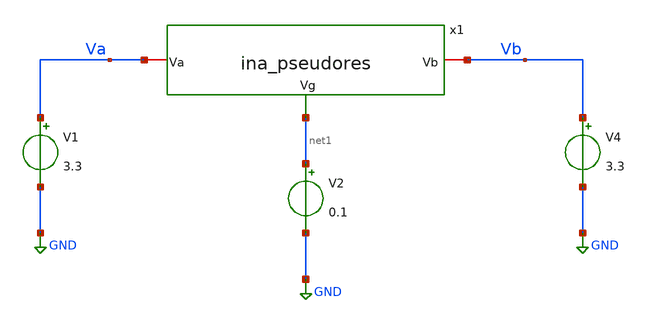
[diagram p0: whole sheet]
** sch_path: designs/libs/tb_ina/tb_ina_pseudores_op/tb_ina_pseudores_op.sch
**.subckt tb_ina_pseudores_op
x1 Va Vb net1 ina_pseudores
V1 Va GND 3.3
V2 net1 GND 0.1
V4 Vb GND 3.3
**** begin user architecture code

.include $::180MCU_MODELS/design.ngspice
.lib $::180MCU_MODELS/sm141064.ngspice typical
.lib $::180MCU_MODELS/sm141064.ngspice cap_mim
.lib $::180MCU_MODELS/sm141064.ngspice moscap_typical
.lib $::180MCU_MODELS/sm141064.ngspice mimcap_typical
.lib $::180MCU_MODELS/sm141064.ngspice res_typical
* .lib $::180MCU_MODELS/sm141064.ngspice res_statistical
* ngspice commands




.control
save all

set color0 = white

*************************************
** PARAMETERS
*************************************

let Vg = 0.1
let Vin = 1.65
let Vout = 1.6511

*************************************
** SOURCES
*************************************

alter @V1[DC] = $&Vin
alter @V2[DC] = $&Vg
alter @V4[DC] = $&Vout

*************************************
** OPERATING POINT SIMULATION
*************************************

op

*************************************
** PRINT RESULTS
*************************************

display
show all

*************************************
** SAVE
*************************************

write tb_ina_pseudores_op.raw

.endc
* ngspice commands



**** end user architecture code
**.ends

* expanding   symbol:  libs/core_ina/ina_pseudores/ina_pseudores.sym # of pins=3
** sym_path: designs/libs/core_ina/ina_pseudores/ina_pseudores.sym
** sch_path: designs/libs/core_ina/ina_pseudores/ina_pseudores.sch
.subckt ina_pseudores Va Vb Vg
*.ipin Vg
*.iopin Va
*.iopin Vb
XM1 Va Vg Vg Vg nfet_03v3 L=5u W=0.28u nf=1 ad='int((nf+1)/2) * W/nf * 0.18u' as='int((nf+2)/2) * W/nf * 0.18u'
+ pd='2*int((nf+1)/2) * (W/nf + 0.18u)' ps='2*int((nf+2)/2) * (W/nf + 0.18u)' nrd='0.18u / W' nrs='0.18u / W'
+ sa=0 sb=0 sd=0 m=1
XM2 net2 Vg Vg Vg nfet_03v3 L=5u W=0.28u nf=1 ad='int((nf+1)/2) * W/nf * 0.18u' as='int((nf+2)/2) * W/nf * 0.18u'
+ pd='2*int((nf+1)/2) * (W/nf + 0.18u)' ps='2*int((nf+2)/2) * (W/nf + 0.18u)' nrd='0.18u / W' nrs='0.18u / W'
+ sa=0 sb=0 sd=0 m=1
XM3 net2 net1 net1 net1 nfet_03v3 L=15u W=0.28u nf=1 ad='int((nf+1)/2) * W/nf * 0.18u' as='int((nf+2)/2) * W/nf * 0.18u'
+ pd='2*int((nf+1)/2) * (W/nf + 0.18u)' ps='2*int((nf+2)/2) * (W/nf + 0.18u)' nrd='0.18u / W' nrs='0.18u / W'
+ sa=0 sb=0 sd=0 m=1
XM4 Vb net1 net1 net1 nfet_03v3 L=15u W=0.28u nf=1 ad='int((nf+1)/2) * W/nf * 0.18u' as='int((nf+2)/2) * W/nf * 0.18u'
+ pd='2*int((nf+1)/2) * (W/nf + 0.18u)' ps='2*int((nf+2)/2) * (W/nf + 0.18u)' nrd='0.18u / W' nrs='0.18u / W'
+ sa=0 sb=0 sd=0 m=1
.ends

.GLOBAL GND
.end
